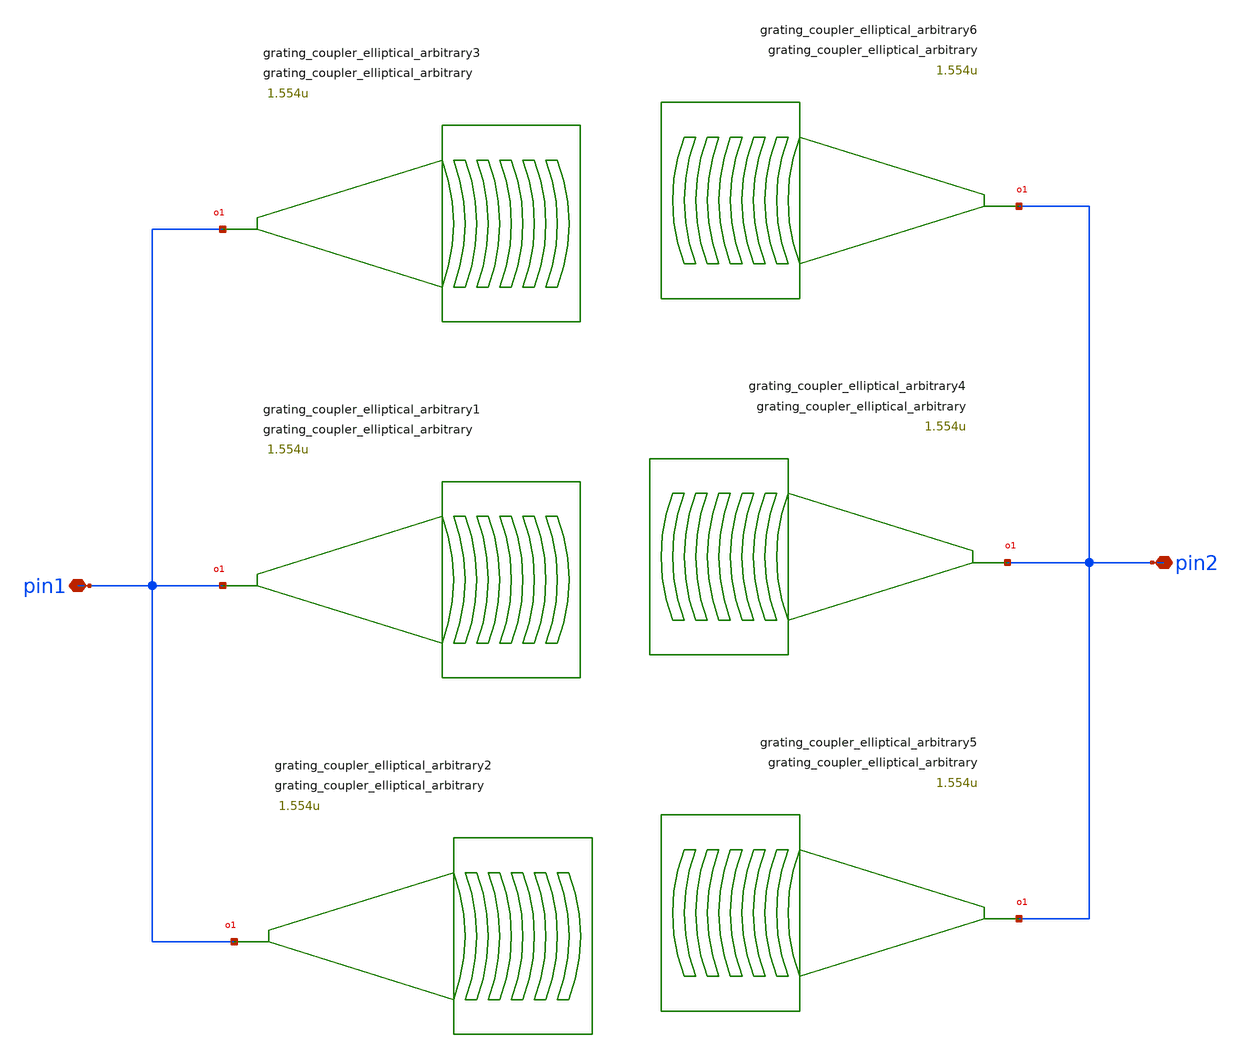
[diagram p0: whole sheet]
** sch_path: xschem/tests/test_sch/test_grating_coupler_elliptical_arbitrary.sch
* Copyright (c) 2024, Mabrains LLC
* Licensed under the GNU Lesser General Public License, Version 3.0 (the "License");
* you may not use this file except in compliance with the License.
* GNU Lesser General Public License
* Version 3, 29 June 2007
* This program is free software: you can redistribute it and/or modify
* it under the terms of the GNU Lesser General Public License as published
* by the Free Software Foundation, either version 3 of the License, or
* (at your option) any later version.
* This program is distributed in the hope that it will be useful,
* but WITHOUT ANY WARRANTY; without even the implied warranty of
* MERCHANTABILITY or FITNESS FOR A PARTICULAR PURPOSE.  See the
* GNU Lesser General Public License for more details.
* You should have received a copy of the GNU Lesser General Public License
* along with this program.  If not, see <https://www.gnu.org/licenses/>.
* SPDX-License-Identifier: LGPL-3.0
**.subckt test_grating_coupler_elliptical_arbitrary pin1 pin2
*.iopin pin1
*.iopin pin2
Pgrating_coupler_elliptical_arbitrary1 pin1 grating_coupler_elliptical_arbitrary gaps=[0.1u, 0.1u,
+ 0.1u, 0.1u, 0.1u, 0.1u, 0.1u, 0.1u, 0.1u, 0.1u] widths=[0.5u, 0.5u, 0.5u, 0.5u, 0.5u, 0.5u, 0.5u, 0.5u,
+ 0.5u, 0.5u] taper_length=16.6u taper_angle=60.0 wavelength=1.554u fiber_angle=15.0
+ taper_to_slab_offset=-3.0u
Pgrating_coupler_elliptical_arbitrary2 pin1 grating_coupler_elliptical_arbitrary gaps=[0.1u, 0.1u,
+ 0.1u, 0.1u, 0.1u, 0.1u, 0.1u, 0.1u, 0.1u, 0.1u] widths=[0.5u, 0.5u, 0.5u, 0.5u, 0.5u, 0.5u, 0.5u, 0.5u,
+ 0.5u, 0.5u] taper_length=16.6u taper_angle=60.0 wavelength=1.554u fiber_angle=15.0
+ taper_to_slab_offset=-3.0u
Pgrating_coupler_elliptical_arbitrary3 pin1 grating_coupler_elliptical_arbitrary gaps=[0.1u, 0.1u,
+ 0.1u, 0.1u, 0.1u, 0.1u, 0.1u, 0.1u, 0.1u, 0.1u] widths=[0.5u, 0.5u, 0.5u, 0.5u, 0.5u, 0.5u, 0.5u, 0.5u,
+ 0.5u, 0.5u] taper_length=16.6u taper_angle=60.0 wavelength=1.554u fiber_angle=15.0
+ taper_to_slab_offset=-3.0u
Pgrating_coupler_elliptical_arbitrary4 pin2 grating_coupler_elliptical_arbitrary gaps=[0.1u, 0.1u,
+ 0.1u, 0.1u, 0.1u, 0.1u, 0.1u, 0.1u, 0.1u, 0.1u] widths=[0.5u, 0.5u, 0.5u, 0.5u, 0.5u, 0.5u, 0.5u, 0.5u,
+ 0.5u, 0.5u] taper_length=16.6u taper_angle=60.0 wavelength=1.554u fiber_angle=15.0
+ taper_to_slab_offset=-3.0u
Pgrating_coupler_elliptical_arbitrary5 pin2 grating_coupler_elliptical_arbitrary gaps=[0.1u, 0.1u,
+ 0.1u, 0.1u, 0.1u, 0.1u, 0.1u, 0.1u, 0.1u, 0.1u] widths=[0.5u, 0.5u, 0.5u, 0.5u, 0.5u, 0.5u, 0.5u, 0.5u,
+ 0.5u, 0.5u] taper_length=16.6u taper_angle=60.0 wavelength=1.554u fiber_angle=15.0
+ taper_to_slab_offset=-3.0u
Pgrating_coupler_elliptical_arbitrary6 pin2 grating_coupler_elliptical_arbitrary gaps=[0.1u, 0.1u,
+ 0.1u, 0.1u, 0.1u, 0.1u, 0.1u, 0.1u, 0.1u, 0.1u] widths=[0.5u, 0.5u, 0.5u, 0.5u, 0.5u, 0.5u, 0.5u, 0.5u,
+ 0.5u, 0.5u] taper_length=16.6u taper_angle=60.0 wavelength=1.554u fiber_angle=15.0
+ taper_to_slab_offset=-3.0u
**.ends
.end
